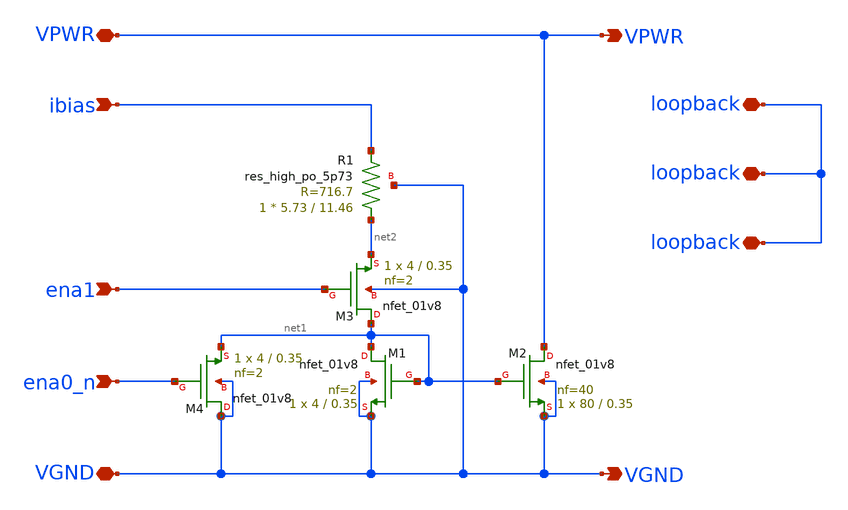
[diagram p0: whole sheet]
** sch_path: xschem/factory_test.sch
**.subckt factory_test ena0_n ena1 VPWR VGND ibias loopback loopback loopback VPWR VGND
*.ipin ena0_n
*.ipin ena1
*.iopin VPWR
*.iopin VGND
*.ipin ibias
*.iopin loopback
*.iopin loopback
*.iopin loopback
*.opin VPWR
*.opin VGND
XM1 net1 net1 VGND VGND sky130_fd_pr__nfet_01v8 L=0.35 W=4 nf=2 ad='int((nf+1)/2) * W/nf * 0.29' as='int((nf+2)/2) * W/nf * 0.29'
+ pd='2*int((nf+1)/2) * (W/nf + 0.29)' ps='2*int((nf+2)/2) * (W/nf + 0.29)' nrd='0.29 / W' nrs='0.29 / W'
+ sa=0 sb=0 sd=0 mult=1 m=1
XM2 VPWR net1 VGND VGND sky130_fd_pr__nfet_01v8 L=0.35 W=80 nf=40 ad='int((nf+1)/2) * W/nf * 0.29' as='int((nf+2)/2) * W/nf * 0.29'
+ pd='2*int((nf+1)/2) * (W/nf + 0.29)' ps='2*int((nf+2)/2) * (W/nf + 0.29)' nrd='0.29 / W' nrs='0.29 / W'
+ sa=0 sb=0 sd=0 mult=1 m=1
XR1 net2 ibias VGND sky130_fd_pr__res_high_po_5p73 L=11.46 mult=1 m=1
XM3 net1 ena1 net2 VGND sky130_fd_pr__nfet_01v8 L=0.35 W=4 nf=2 ad='int((nf+1)/2) * W/nf * 0.29' as='int((nf+2)/2) * W/nf * 0.29'
+ pd='2*int((nf+1)/2) * (W/nf + 0.29)' ps='2*int((nf+2)/2) * (W/nf + 0.29)' nrd='0.29 / W' nrs='0.29 / W'
+ sa=0 sb=0 sd=0 mult=1 m=1
XM4 VGND ena0_n net1 VGND sky130_fd_pr__nfet_01v8 L=0.35 W=4 nf=2 ad='int((nf+1)/2) * W/nf * 0.29' as='int((nf+2)/2) * W/nf * 0.29'
+ pd='2*int((nf+1)/2) * (W/nf + 0.29)' ps='2*int((nf+2)/2) * (W/nf + 0.29)' nrd='0.29 / W' nrs='0.29 / W'
+ sa=0 sb=0 sd=0 mult=1 m=1
**.ends
.end
